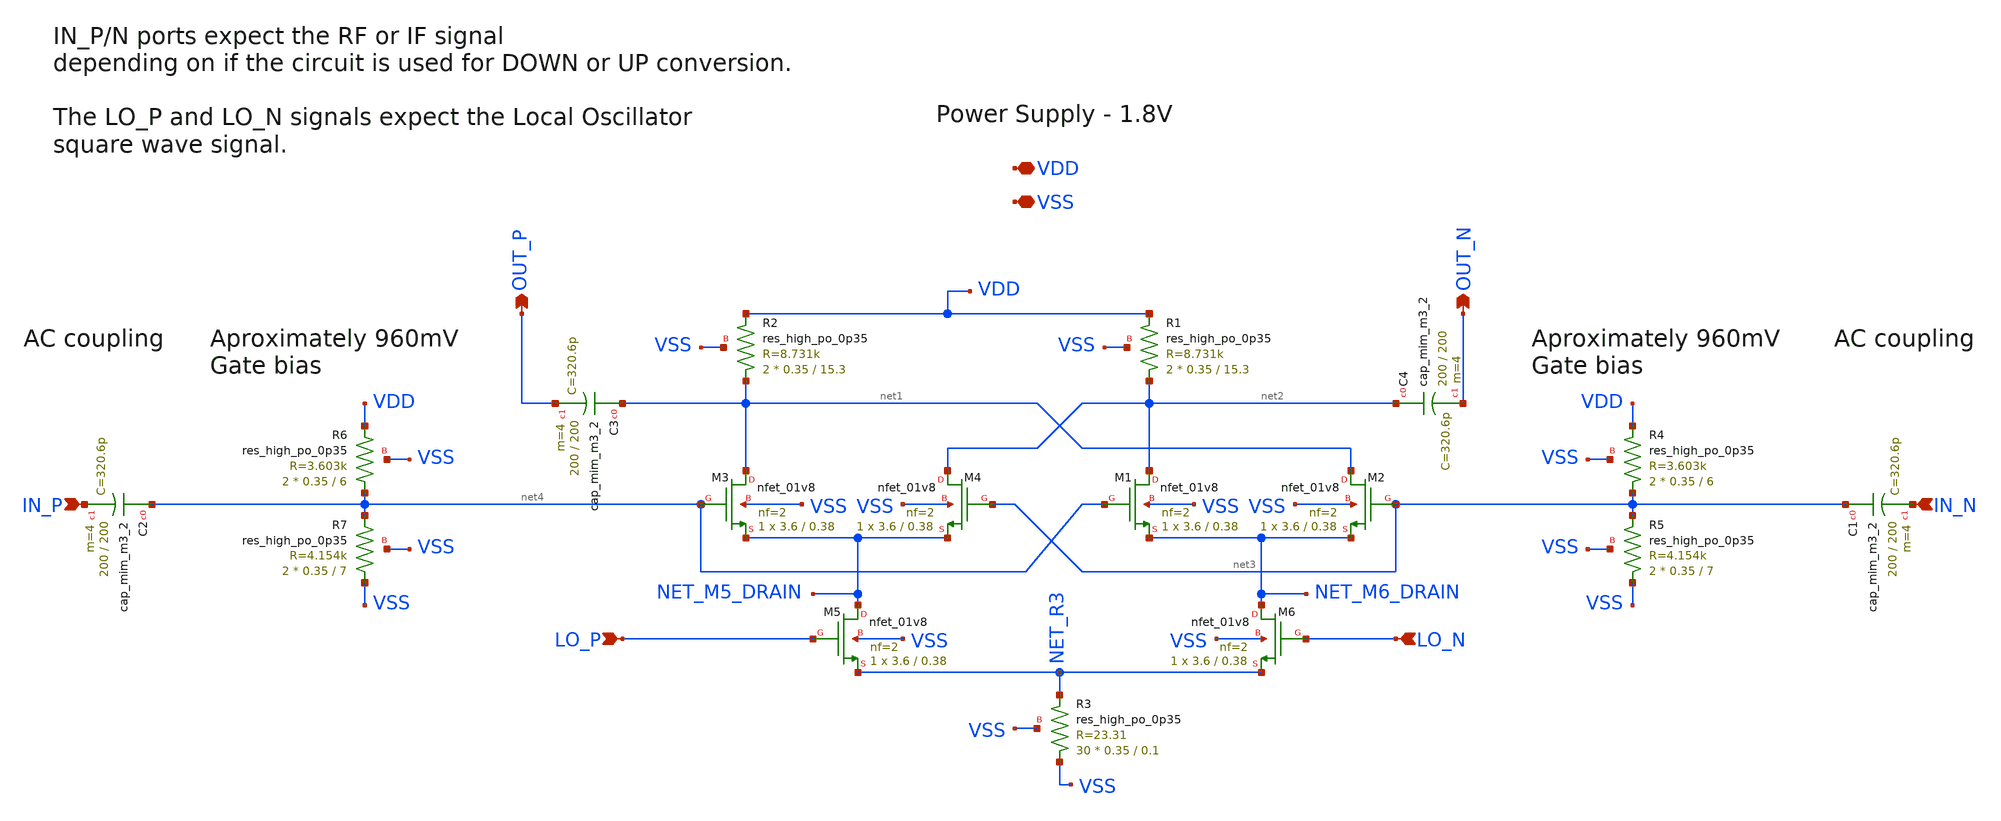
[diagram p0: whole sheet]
** sch_path: xschem/gilbert_mixer.sch
**.subckt gilbert_mixer LO_P LO_N IN_N OUT_N OUT_P VDD VSS IN_P
*.ipin LO_P
*.ipin LO_N
*.ipin IN_N
*.opin OUT_N
*.opin OUT_P
*.iopin VDD
*.iopin VSS
*.ipin IN_P
XR3 VSS NET_R3 VSS sky130_fd_pr__res_high_po_0p35 L=0.1 mult=30 m=30
XM2 net1 net3 NET_M6_DRAIN VSS sky130_fd_pr__nfet_01v8 L=0.38 W=3.6 nf=2 ad='int((nf+1)/2) * W/nf * 0.29'
+ as='int((nf+2)/2) * W/nf * 0.29' pd='2*int((nf+1)/2) * (W/nf + 0.29)' ps='2*int((nf+2)/2) * (W/nf + 0.29)'
+ nrd='0.29 / W' nrs='0.29 / W' sa=0 sb=0 sd=0 mult=1 m=1
XM4 net2 net3 NET_M5_DRAIN VSS sky130_fd_pr__nfet_01v8 L=0.38 W=3.6 nf=2 ad='int((nf+1)/2) * W/nf * 0.29'
+ as='int((nf+2)/2) * W/nf * 0.29' pd='2*int((nf+1)/2) * (W/nf + 0.29)' ps='2*int((nf+2)/2) * (W/nf + 0.29)'
+ nrd='0.29 / W' nrs='0.29 / W' sa=0 sb=0 sd=0 mult=1 m=1
XM6 NET_M6_DRAIN LO_N NET_R3 VSS sky130_fd_pr__nfet_01v8 L=0.38 W=3.6 nf=2 ad='int((nf+1)/2) * W/nf * 0.29'
+ as='int((nf+2)/2) * W/nf * 0.29' pd='2*int((nf+1)/2) * (W/nf + 0.29)' ps='2*int((nf+2)/2) * (W/nf + 0.29)'
+ nrd='0.29 / W' nrs='0.29 / W' sa=0 sb=0 sd=0 mult=1 m=1
XM1 net2 net4 NET_M6_DRAIN VSS sky130_fd_pr__nfet_01v8 L=0.38 W=3.6 nf=2 ad='int((nf+1)/2) * W/nf * 0.29'
+ as='int((nf+2)/2) * W/nf * 0.29' pd='2*int((nf+1)/2) * (W/nf + 0.29)' ps='2*int((nf+2)/2) * (W/nf + 0.29)'
+ nrd='0.29 / W' nrs='0.29 / W' sa=0 sb=0 sd=0 mult=1 m=1
XM3 net1 net4 NET_M5_DRAIN VSS sky130_fd_pr__nfet_01v8 L=0.38 W=3.6 nf=2 ad='int((nf+1)/2) * W/nf * 0.29'
+ as='int((nf+2)/2) * W/nf * 0.29' pd='2*int((nf+1)/2) * (W/nf + 0.29)' ps='2*int((nf+2)/2) * (W/nf + 0.29)'
+ nrd='0.29 / W' nrs='0.29 / W' sa=0 sb=0 sd=0 mult=1 m=1
XM5 NET_M5_DRAIN LO_P NET_R3 VSS sky130_fd_pr__nfet_01v8 L=0.38 W=3.6 nf=2 ad='int((nf+1)/2) * W/nf * 0.29'
+ as='int((nf+2)/2) * W/nf * 0.29' pd='2*int((nf+1)/2) * (W/nf + 0.29)' ps='2*int((nf+2)/2) * (W/nf + 0.29)'
+ nrd='0.29 / W' nrs='0.29 / W' sa=0 sb=0 sd=0 mult=1 m=1
XR1 net2 VDD VSS sky130_fd_pr__res_high_po_0p35 L=15.3 mult=2 m=2
XR2 net1 VDD VSS sky130_fd_pr__res_high_po_0p35 L=15.3 mult=2 m=2
XR4 net3 VDD VSS sky130_fd_pr__res_high_po_0p35 L=6 mult=2 m=2
XR5 VSS net3 VSS sky130_fd_pr__res_high_po_0p35 L=7 mult=2 m=2
XC1 net3 IN_N sky130_fd_pr__cap_mim_m3_2 W=200 L=200 MF=4 m=4
XR6 net4 VDD VSS sky130_fd_pr__res_high_po_0p35 L=6 mult=2 m=2
XR7 VSS net4 VSS sky130_fd_pr__res_high_po_0p35 L=7 mult=2 m=2
XC2 net4 IN_P sky130_fd_pr__cap_mim_m3_2 W=200 L=200 MF=4 m=4
XC3 net1 OUT_P sky130_fd_pr__cap_mim_m3_2 W=200 L=200 MF=4 m=4
XC4 net2 OUT_N sky130_fd_pr__cap_mim_m3_2 W=200 L=200 MF=4 m=4
**.ends
.end
